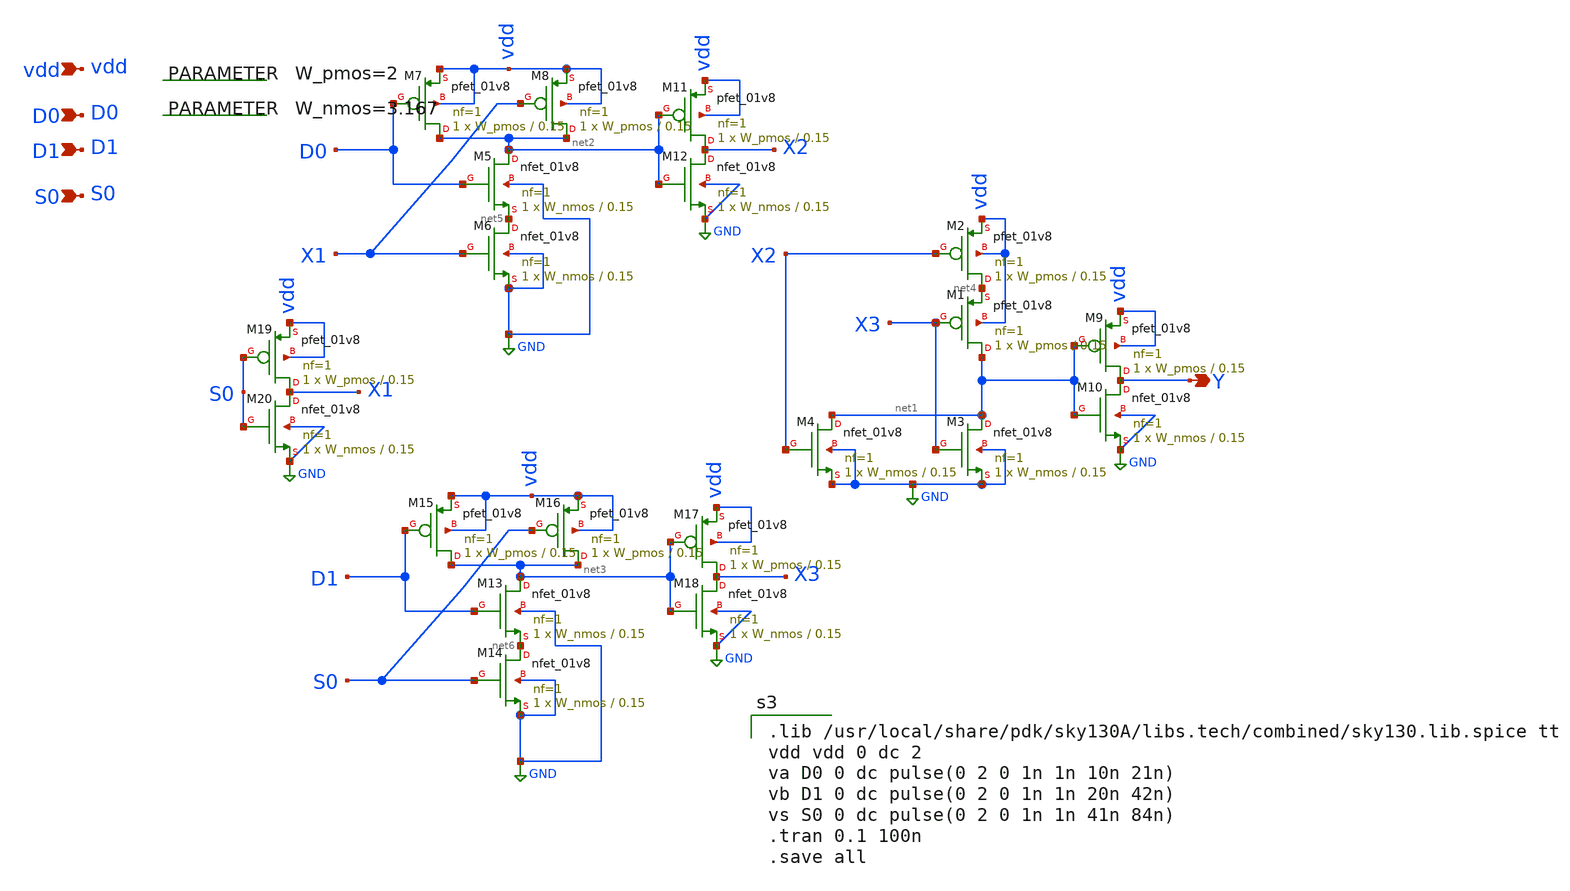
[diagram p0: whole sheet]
** sch_path: Circuit Files/circuits/circuits/2_1M_MR.sch
**.subckt 2_1M_MR D0 D1 vdd S0 Y
*.ipin D0
*.ipin D1
*.ipin vdd
*.ipin S0
*.opin Y
XM1 net1 X3 net4 vdd sky130_fd_pr__pfet_01v8 L=0.15 W=W_pmos nf=1 ad='int((nf+1)/2) * W/nf * 0.29' as='int((nf+2)/2) * W/nf * 0.29'
+ pd='2*int((nf+1)/2) * (W/nf + 0.29)' ps='2*int((nf+2)/2) * (W/nf + 0.29)' nrd='0.29 / W' nrs='0.29 / W'
+ sa=0 sb=0 sd=0 mult=1 m=1
XM2 net4 X2 vdd vdd sky130_fd_pr__pfet_01v8 L=0.15 W=W_pmos nf=1 ad='int((nf+1)/2) * W/nf * 0.29' as='int((nf+2)/2) * W/nf * 0.29'
+ pd='2*int((nf+1)/2) * (W/nf + 0.29)' ps='2*int((nf+2)/2) * (W/nf + 0.29)' nrd='0.29 / W' nrs='0.29 / W'
+ sa=0 sb=0 sd=0 mult=1 m=1
XM3 net1 X3 GND GND sky130_fd_pr__nfet_01v8 L=0.15 W=W_nmos nf=1 ad='int((nf+1)/2) * W/nf * 0.29' as='int((nf+2)/2) * W/nf * 0.29'
+ pd='2*int((nf+1)/2) * (W/nf + 0.29)' ps='2*int((nf+2)/2) * (W/nf + 0.29)' nrd='0.29 / W' nrs='0.29 / W'
+ sa=0 sb=0 sd=0 mult=1 m=1
XM4 net1 X2 GND GND sky130_fd_pr__nfet_01v8 L=0.15 W=W_nmos nf=1 ad='int((nf+1)/2) * W/nf * 0.29' as='int((nf+2)/2) * W/nf * 0.29'
+ pd='2*int((nf+1)/2) * (W/nf + 0.29)' ps='2*int((nf+2)/2) * (W/nf + 0.29)' nrd='0.29 / W' nrs='0.29 / W'
+ sa=0 sb=0 sd=0 mult=1 m=1
XM9 Y net1 vdd vdd sky130_fd_pr__pfet_01v8 L=0.15 W=W_pmos nf=1 ad='int((nf+1)/2) * W/nf * 0.29' as='int((nf+2)/2) * W/nf * 0.29'
+ pd='2*int((nf+1)/2) * (W/nf + 0.29)' ps='2*int((nf+2)/2) * (W/nf + 0.29)' nrd='0.29 / W' nrs='0.29 / W'
+ sa=0 sb=0 sd=0 mult=1 m=1
XM10 Y net1 GND GND sky130_fd_pr__nfet_01v8 L=0.15 W=W_nmos nf=1 ad='int((nf+1)/2) * W/nf * 0.29' as='int((nf+2)/2) * W/nf * 0.29'
+ pd='2*int((nf+1)/2) * (W/nf + 0.29)' ps='2*int((nf+2)/2) * (W/nf + 0.29)' nrd='0.29 / W' nrs='0.29 / W'
+ sa=0 sb=0 sd=0 mult=1 m=1
XM5 net2 D0 net5 GND sky130_fd_pr__nfet_01v8 L=0.15 W=W_nmos nf=1 ad='int((nf+1)/2) * W/nf * 0.29' as='int((nf+2)/2) * W/nf * 0.29'
+ pd='2*int((nf+1)/2) * (W/nf + 0.29)' ps='2*int((nf+2)/2) * (W/nf + 0.29)' nrd='0.29 / W' nrs='0.29 / W'
+ sa=0 sb=0 sd=0 mult=1 m=1
XM6 net5 X1 GND GND sky130_fd_pr__nfet_01v8 L=0.15 W=W_nmos nf=1 ad='int((nf+1)/2) * W/nf * 0.29' as='int((nf+2)/2) * W/nf * 0.29'
+ pd='2*int((nf+1)/2) * (W/nf + 0.29)' ps='2*int((nf+2)/2) * (W/nf + 0.29)' nrd='0.29 / W' nrs='0.29 / W'
+ sa=0 sb=0 sd=0 mult=1 m=1
XM7 net2 D0 vdd vdd sky130_fd_pr__pfet_01v8 L=0.15 W=W_pmos nf=1 ad='int((nf+1)/2) * W/nf * 0.29' as='int((nf+2)/2) * W/nf * 0.29'
+ pd='2*int((nf+1)/2) * (W/nf + 0.29)' ps='2*int((nf+2)/2) * (W/nf + 0.29)' nrd='0.29 / W' nrs='0.29 / W'
+ sa=0 sb=0 sd=0 mult=1 m=1
XM8 net2 X1 vdd vdd sky130_fd_pr__pfet_01v8 L=0.15 W=W_pmos nf=1 ad='int((nf+1)/2) * W/nf * 0.29' as='int((nf+2)/2) * W/nf * 0.29'
+ pd='2*int((nf+1)/2) * (W/nf + 0.29)' ps='2*int((nf+2)/2) * (W/nf + 0.29)' nrd='0.29 / W' nrs='0.29 / W'
+ sa=0 sb=0 sd=0 mult=1 m=1
XM11 X2 net2 vdd vdd sky130_fd_pr__pfet_01v8 L=0.15 W=W_pmos nf=1 ad='int((nf+1)/2) * W/nf * 0.29' as='int((nf+2)/2) * W/nf * 0.29'
+ pd='2*int((nf+1)/2) * (W/nf + 0.29)' ps='2*int((nf+2)/2) * (W/nf + 0.29)' nrd='0.29 / W' nrs='0.29 / W'
+ sa=0 sb=0 sd=0 mult=1 m=1
XM12 X2 net2 GND GND sky130_fd_pr__nfet_01v8 L=0.15 W=W_nmos nf=1 ad='int((nf+1)/2) * W/nf * 0.29' as='int((nf+2)/2) * W/nf * 0.29'
+ pd='2*int((nf+1)/2) * (W/nf + 0.29)' ps='2*int((nf+2)/2) * (W/nf + 0.29)' nrd='0.29 / W' nrs='0.29 / W'
+ sa=0 sb=0 sd=0 mult=1 m=1
XM13 net3 D1 net6 GND sky130_fd_pr__nfet_01v8 L=0.15 W=W_nmos nf=1 ad='int((nf+1)/2) * W/nf * 0.29' as='int((nf+2)/2) * W/nf * 0.29'
+ pd='2*int((nf+1)/2) * (W/nf + 0.29)' ps='2*int((nf+2)/2) * (W/nf + 0.29)' nrd='0.29 / W' nrs='0.29 / W'
+ sa=0 sb=0 sd=0 mult=1 m=1
XM14 net6 S0 GND GND sky130_fd_pr__nfet_01v8 L=0.15 W=W_nmos nf=1 ad='int((nf+1)/2) * W/nf * 0.29' as='int((nf+2)/2) * W/nf * 0.29'
+ pd='2*int((nf+1)/2) * (W/nf + 0.29)' ps='2*int((nf+2)/2) * (W/nf + 0.29)' nrd='0.29 / W' nrs='0.29 / W'
+ sa=0 sb=0 sd=0 mult=1 m=1
XM15 net3 D1 vdd vdd sky130_fd_pr__pfet_01v8 L=0.15 W=W_pmos nf=1 ad='int((nf+1)/2) * W/nf * 0.29' as='int((nf+2)/2) * W/nf * 0.29'
+ pd='2*int((nf+1)/2) * (W/nf + 0.29)' ps='2*int((nf+2)/2) * (W/nf + 0.29)' nrd='0.29 / W' nrs='0.29 / W'
+ sa=0 sb=0 sd=0 mult=1 m=1
XM16 net3 S0 vdd vdd sky130_fd_pr__pfet_01v8 L=0.15 W=W_pmos nf=1 ad='int((nf+1)/2) * W/nf * 0.29' as='int((nf+2)/2) * W/nf * 0.29'
+ pd='2*int((nf+1)/2) * (W/nf + 0.29)' ps='2*int((nf+2)/2) * (W/nf + 0.29)' nrd='0.29 / W' nrs='0.29 / W'
+ sa=0 sb=0 sd=0 mult=1 m=1
XM17 X3 net3 vdd vdd sky130_fd_pr__pfet_01v8 L=0.15 W=W_pmos nf=1 ad='int((nf+1)/2) * W/nf * 0.29' as='int((nf+2)/2) * W/nf * 0.29'
+ pd='2*int((nf+1)/2) * (W/nf + 0.29)' ps='2*int((nf+2)/2) * (W/nf + 0.29)' nrd='0.29 / W' nrs='0.29 / W'
+ sa=0 sb=0 sd=0 mult=1 m=1
XM18 X3 net3 GND GND sky130_fd_pr__nfet_01v8 L=0.15 W=W_nmos nf=1 ad='int((nf+1)/2) * W/nf * 0.29' as='int((nf+2)/2) * W/nf * 0.29'
+ pd='2*int((nf+1)/2) * (W/nf + 0.29)' ps='2*int((nf+2)/2) * (W/nf + 0.29)' nrd='0.29 / W' nrs='0.29 / W'
+ sa=0 sb=0 sd=0 mult=1 m=1
XM19 X1 S0 vdd vdd sky130_fd_pr__pfet_01v8 L=0.15 W=W_pmos nf=1 ad='int((nf+1)/2) * W/nf * 0.29' as='int((nf+2)/2) * W/nf * 0.29'
+ pd='2*int((nf+1)/2) * (W/nf + 0.29)' ps='2*int((nf+2)/2) * (W/nf + 0.29)' nrd='0.29 / W' nrs='0.29 / W'
+ sa=0 sb=0 sd=0 mult=1 m=1
XM20 X1 S0 GND GND sky130_fd_pr__nfet_01v8 L=0.15 W=W_nmos nf=1 ad='int((nf+1)/2) * W/nf * 0.29' as='int((nf+2)/2) * W/nf * 0.29'
+ pd='2*int((nf+1)/2) * (W/nf + 0.29)' ps='2*int((nf+2)/2) * (W/nf + 0.29)' nrd='0.29 / W' nrs='0.29 / W'
+ sa=0 sb=0 sd=0 mult=1 m=1
.param W_pmos=2
.param W_nmos=3.167
**** begin user architecture code

.lib /usr/local/share/pdk/sky130A/libs.tech/combined/sky130.lib.spice tt
vdd vdd 0 dc 2
va D0 0 dc pulse(0 2 0 1n 1n 10n 21n)
vb D1 0 dc pulse(0 2 0 1n 1n 20n 42n)
vs S0 0 dc pulse(0 2 0 1n 1n 41n 84n)
.tran 0.1 100n
.save all

**** end user architecture code
**.ends
.GLOBAL GND
.end
